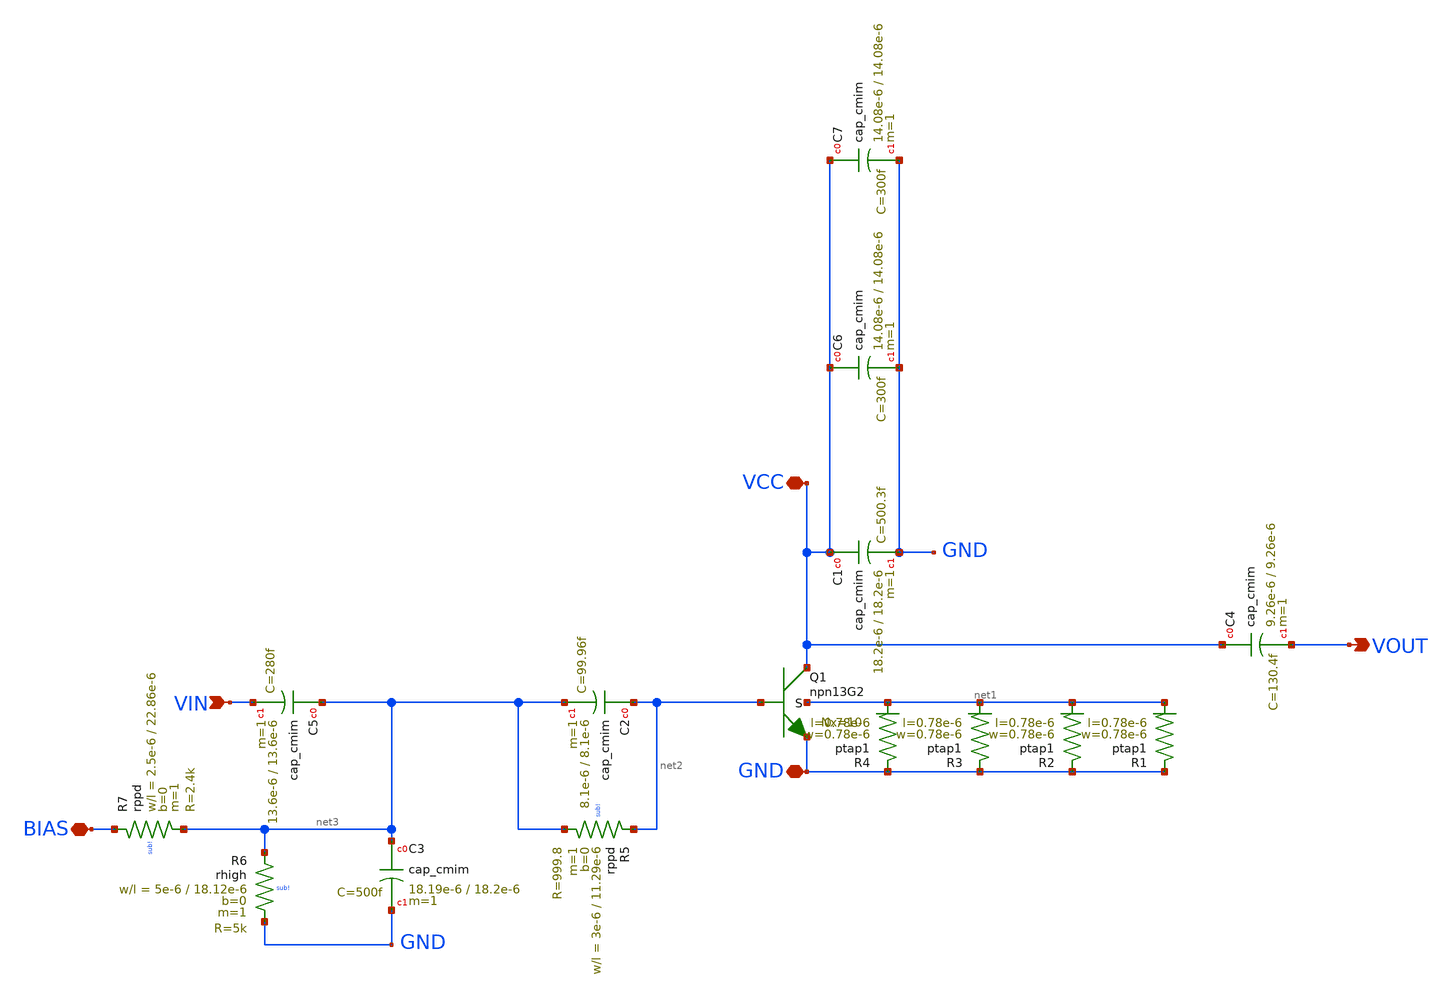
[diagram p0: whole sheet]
** sch_path: 60_GHZ_MPA/design_data/lvs/60_ghz_mpa.sch
**.subckt 60_ghz_mpa VCC GND BIAS VIN VOUT
*.iopin VCC
*.iopin GND
*.iopin BIAS
*.ipin VIN
*.opin VOUT
XQ1 VCC net2 GND net1 npn13G2 Nx=10 mm_ok=1
XR1 GND net1 ptap1 R=262.8 w=0.78e-6 l=0.78e-6
XR2 GND net1 ptap1 R=262.8 w=0.78e-6 l=0.78e-6
XR3 GND net1 ptap1 R=262.8 w=0.78e-6 l=0.78e-6
XR4 GND net1 ptap1 R=262.8 w=0.78e-6 l=0.78e-6
XC1 VCC GND cap_cmim w=18.2e-6 l=18.2e-6 m=1 mm_ok=1
XC2 net2 net3 cap_cmim w=8.1e-6 l=8.1e-6 m=1 mm_ok=1
XR5 net2 net3 sub! rppd w=3e-6 l=11.29e-6 m=1 b=0 mm_ok=1
XC3 net3 GND cap_cmim w=18.19e-6 l=18.2e-6 m=1 mm_ok=1
XR7 BIAS net3 sub! rppd w=2.5e-6 l=22.86e-6 m=1 b=0 mm_ok=1
XC4 VCC VOUT cap_cmim w=9.26e-6 l=9.26e-6 m=1 mm_ok=1
XR6 net3 GND sub! rhigh w=5e-6 l=18.12e-6 m=1 b=0 mm_ok=1
XC5 net3 VIN cap_cmim w=13.6e-6 l=13.6e-6 m=1 mm_ok=1
XC6 VCC GND cap_cmim w=14.08e-6 l=14.08e-6 m=1 mm_ok=1
XC7 VCC GND cap_cmim w=14.08e-6 l=14.08e-6 m=1 mm_ok=1
**.ends
.end
